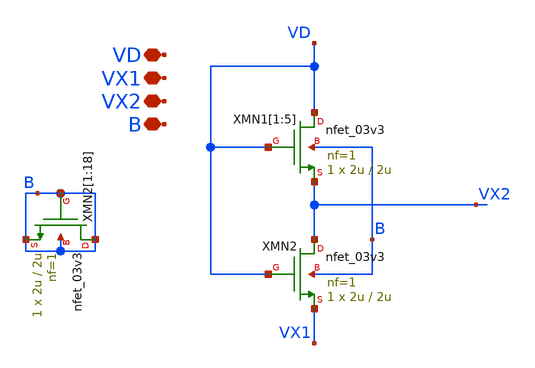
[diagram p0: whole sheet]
** sch_path: Voltage_Reference/symbols_vr/SCM_VR.sch
**.subckt SCM_VR VD VX1 VX2 B
*.iopin VD
*.iopin VX1
*.iopin VX2
*.iopin B
XMN1[1] VD VD VX2 B nfet_03v3 L=2u W=2u nf=1 ad='int((nf+1)/2) * W/nf * 0.18u' as='int((nf+2)/2) * W/nf * 0.18u'
+ pd='2*int((nf+1)/2) * (W/nf + 0.18u)' ps='2*int((nf+2)/2) * (W/nf + 0.18u)' nrd='0.18u / W' nrs='0.18u / W'
+ sa=0 sb=0 sd=0 m=1
XMN1[2] VD VD VX2 B nfet_03v3 L=2u W=2u nf=1 ad='int((nf+1)/2) * W/nf * 0.18u' as='int((nf+2)/2) * W/nf * 0.18u'
+ pd='2*int((nf+1)/2) * (W/nf + 0.18u)' ps='2*int((nf+2)/2) * (W/nf + 0.18u)' nrd='0.18u / W' nrs='0.18u / W'
+ sa=0 sb=0 sd=0 m=1
XMN1[3] VD VD VX2 B nfet_03v3 L=2u W=2u nf=1 ad='int((nf+1)/2) * W/nf * 0.18u' as='int((nf+2)/2) * W/nf * 0.18u'
+ pd='2*int((nf+1)/2) * (W/nf + 0.18u)' ps='2*int((nf+2)/2) * (W/nf + 0.18u)' nrd='0.18u / W' nrs='0.18u / W'
+ sa=0 sb=0 sd=0 m=1
XMN1[4] VD VD VX2 B nfet_03v3 L=2u W=2u nf=1 ad='int((nf+1)/2) * W/nf * 0.18u' as='int((nf+2)/2) * W/nf * 0.18u'
+ pd='2*int((nf+1)/2) * (W/nf + 0.18u)' ps='2*int((nf+2)/2) * (W/nf + 0.18u)' nrd='0.18u / W' nrs='0.18u / W'
+ sa=0 sb=0 sd=0 m=1
XMN1[5] VD VD VX2 B nfet_03v3 L=2u W=2u nf=1 ad='int((nf+1)/2) * W/nf * 0.18u' as='int((nf+2)/2) * W/nf * 0.18u'
+ pd='2*int((nf+1)/2) * (W/nf + 0.18u)' ps='2*int((nf+2)/2) * (W/nf + 0.18u)' nrd='0.18u / W' nrs='0.18u / W'
+ sa=0 sb=0 sd=0 m=1
XMN2 VX2 VD VX1 B nfet_03v3 L=2u W=2u nf=1 ad='int((nf+1)/2) * W/nf * 0.18u' as='int((nf+2)/2) * W/nf * 0.18u'
+ pd='2*int((nf+1)/2) * (W/nf + 0.18u)' ps='2*int((nf+2)/2) * (W/nf + 0.18u)' nrd='0.18u / W' nrs='0.18u / W'
+ sa=0 sb=0 sd=0 m=1
XMN2[1] B B B B nfet_03v3 L=2u W=2u nf=1 ad='int((nf+1)/2) * W/nf * 0.18u' as='int((nf+2)/2) * W/nf * 0.18u'
+ pd='2*int((nf+1)/2) * (W/nf + 0.18u)' ps='2*int((nf+2)/2) * (W/nf + 0.18u)' nrd='0.18u / W' nrs='0.18u / W'
+ sa=0 sb=0 sd=0 m=1
XMN2[2] B B B B nfet_03v3 L=2u W=2u nf=1 ad='int((nf+1)/2) * W/nf * 0.18u' as='int((nf+2)/2) * W/nf * 0.18u'
+ pd='2*int((nf+1)/2) * (W/nf + 0.18u)' ps='2*int((nf+2)/2) * (W/nf + 0.18u)' nrd='0.18u / W' nrs='0.18u / W'
+ sa=0 sb=0 sd=0 m=1
XMN2[3] B B B B nfet_03v3 L=2u W=2u nf=1 ad='int((nf+1)/2) * W/nf * 0.18u' as='int((nf+2)/2) * W/nf * 0.18u'
+ pd='2*int((nf+1)/2) * (W/nf + 0.18u)' ps='2*int((nf+2)/2) * (W/nf + 0.18u)' nrd='0.18u / W' nrs='0.18u / W'
+ sa=0 sb=0 sd=0 m=1
XMN2[4] B B B B nfet_03v3 L=2u W=2u nf=1 ad='int((nf+1)/2) * W/nf * 0.18u' as='int((nf+2)/2) * W/nf * 0.18u'
+ pd='2*int((nf+1)/2) * (W/nf + 0.18u)' ps='2*int((nf+2)/2) * (W/nf + 0.18u)' nrd='0.18u / W' nrs='0.18u / W'
+ sa=0 sb=0 sd=0 m=1
XMN2[5] B B B B nfet_03v3 L=2u W=2u nf=1 ad='int((nf+1)/2) * W/nf * 0.18u' as='int((nf+2)/2) * W/nf * 0.18u'
+ pd='2*int((nf+1)/2) * (W/nf + 0.18u)' ps='2*int((nf+2)/2) * (W/nf + 0.18u)' nrd='0.18u / W' nrs='0.18u / W'
+ sa=0 sb=0 sd=0 m=1
XMN2[6] B B B B nfet_03v3 L=2u W=2u nf=1 ad='int((nf+1)/2) * W/nf * 0.18u' as='int((nf+2)/2) * W/nf * 0.18u'
+ pd='2*int((nf+1)/2) * (W/nf + 0.18u)' ps='2*int((nf+2)/2) * (W/nf + 0.18u)' nrd='0.18u / W' nrs='0.18u / W'
+ sa=0 sb=0 sd=0 m=1
XMN2[7] B B B B nfet_03v3 L=2u W=2u nf=1 ad='int((nf+1)/2) * W/nf * 0.18u' as='int((nf+2)/2) * W/nf * 0.18u'
+ pd='2*int((nf+1)/2) * (W/nf + 0.18u)' ps='2*int((nf+2)/2) * (W/nf + 0.18u)' nrd='0.18u / W' nrs='0.18u / W'
+ sa=0 sb=0 sd=0 m=1
XMN2[8] B B B B nfet_03v3 L=2u W=2u nf=1 ad='int((nf+1)/2) * W/nf * 0.18u' as='int((nf+2)/2) * W/nf * 0.18u'
+ pd='2*int((nf+1)/2) * (W/nf + 0.18u)' ps='2*int((nf+2)/2) * (W/nf + 0.18u)' nrd='0.18u / W' nrs='0.18u / W'
+ sa=0 sb=0 sd=0 m=1
XMN2[9] B B B B nfet_03v3 L=2u W=2u nf=1 ad='int((nf+1)/2) * W/nf * 0.18u' as='int((nf+2)/2) * W/nf * 0.18u'
+ pd='2*int((nf+1)/2) * (W/nf + 0.18u)' ps='2*int((nf+2)/2) * (W/nf + 0.18u)' nrd='0.18u / W' nrs='0.18u / W'
+ sa=0 sb=0 sd=0 m=1
XMN2[10] B B B B nfet_03v3 L=2u W=2u nf=1 ad='int((nf+1)/2) * W/nf * 0.18u' as='int((nf+2)/2) * W/nf * 0.18u'
+ pd='2*int((nf+1)/2) * (W/nf + 0.18u)' ps='2*int((nf+2)/2) * (W/nf + 0.18u)' nrd='0.18u / W' nrs='0.18u / W'
+ sa=0 sb=0 sd=0 m=1
XMN2[11] B B B B nfet_03v3 L=2u W=2u nf=1 ad='int((nf+1)/2) * W/nf * 0.18u' as='int((nf+2)/2) * W/nf * 0.18u'
+ pd='2*int((nf+1)/2) * (W/nf + 0.18u)' ps='2*int((nf+2)/2) * (W/nf + 0.18u)' nrd='0.18u / W' nrs='0.18u / W'
+ sa=0 sb=0 sd=0 m=1
XMN2[12] B B B B nfet_03v3 L=2u W=2u nf=1 ad='int((nf+1)/2) * W/nf * 0.18u' as='int((nf+2)/2) * W/nf * 0.18u'
+ pd='2*int((nf+1)/2) * (W/nf + 0.18u)' ps='2*int((nf+2)/2) * (W/nf + 0.18u)' nrd='0.18u / W' nrs='0.18u / W'
+ sa=0 sb=0 sd=0 m=1
XMN2[13] B B B B nfet_03v3 L=2u W=2u nf=1 ad='int((nf+1)/2) * W/nf * 0.18u' as='int((nf+2)/2) * W/nf * 0.18u'
+ pd='2*int((nf+1)/2) * (W/nf + 0.18u)' ps='2*int((nf+2)/2) * (W/nf + 0.18u)' nrd='0.18u / W' nrs='0.18u / W'
+ sa=0 sb=0 sd=0 m=1
XMN2[14] B B B B nfet_03v3 L=2u W=2u nf=1 ad='int((nf+1)/2) * W/nf * 0.18u' as='int((nf+2)/2) * W/nf * 0.18u'
+ pd='2*int((nf+1)/2) * (W/nf + 0.18u)' ps='2*int((nf+2)/2) * (W/nf + 0.18u)' nrd='0.18u / W' nrs='0.18u / W'
+ sa=0 sb=0 sd=0 m=1
XMN2[15] B B B B nfet_03v3 L=2u W=2u nf=1 ad='int((nf+1)/2) * W/nf * 0.18u' as='int((nf+2)/2) * W/nf * 0.18u'
+ pd='2*int((nf+1)/2) * (W/nf + 0.18u)' ps='2*int((nf+2)/2) * (W/nf + 0.18u)' nrd='0.18u / W' nrs='0.18u / W'
+ sa=0 sb=0 sd=0 m=1
XMN2[16] B B B B nfet_03v3 L=2u W=2u nf=1 ad='int((nf+1)/2) * W/nf * 0.18u' as='int((nf+2)/2) * W/nf * 0.18u'
+ pd='2*int((nf+1)/2) * (W/nf + 0.18u)' ps='2*int((nf+2)/2) * (W/nf + 0.18u)' nrd='0.18u / W' nrs='0.18u / W'
+ sa=0 sb=0 sd=0 m=1
XMN2[17] B B B B nfet_03v3 L=2u W=2u nf=1 ad='int((nf+1)/2) * W/nf * 0.18u' as='int((nf+2)/2) * W/nf * 0.18u'
+ pd='2*int((nf+1)/2) * (W/nf + 0.18u)' ps='2*int((nf+2)/2) * (W/nf + 0.18u)' nrd='0.18u / W' nrs='0.18u / W'
+ sa=0 sb=0 sd=0 m=1
XMN2[18] B B B B nfet_03v3 L=2u W=2u nf=1 ad='int((nf+1)/2) * W/nf * 0.18u' as='int((nf+2)/2) * W/nf * 0.18u'
+ pd='2*int((nf+1)/2) * (W/nf + 0.18u)' ps='2*int((nf+2)/2) * (W/nf + 0.18u)' nrd='0.18u / W' nrs='0.18u / W'
+ sa=0 sb=0 sd=0 m=1
**.ends
.end
